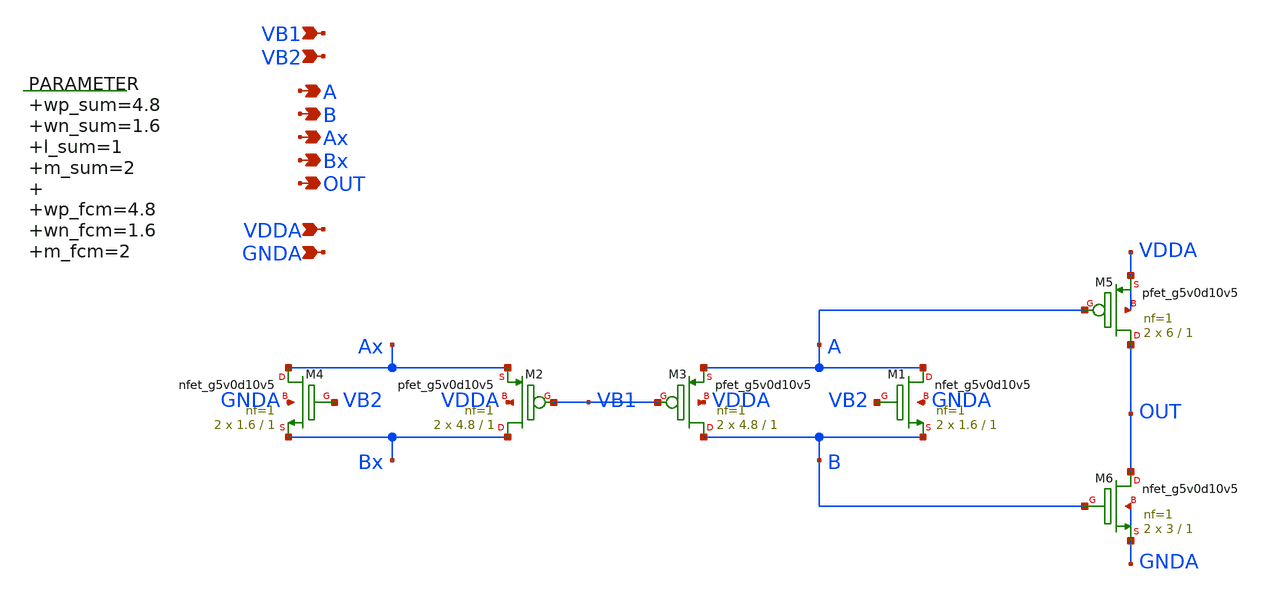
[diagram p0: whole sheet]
** sch_path: xschem/monticelli_top.sch
**.subckt monticelli_top A B VDDA GNDA Ax Bx VB1 VB2 OUT
*.opin A
*.opin B
*.ipin VDDA
*.ipin GNDA
*.opin Ax
*.opin Bx
*.ipin VB1
*.ipin VB2
*.opin OUT
.param wp_sum=4.8 wn_sum=1.6 l_sum=1 m_sum=2 wp_fcm=4.8 wn_fcm=1.6 m_fcm=2

XM1 A VB2 B GNDA sky130_fd_pr__nfet_g5v0d10v5 L=1 W=1.6 nf=1 ad='int((nf+1)/2) * W/nf * 0.29' as='int((nf+2)/2) * W/nf * 0.29'
+ pd='2*int((nf+1)/2) * (W/nf + 0.29)' ps='2*int((nf+2)/2) * (W/nf + 0.29)' nrd='0.29 / W' nrs='0.29 / W'
+ sa=0 sb=0 sd=0 mult=2 m=2
XM2 Bx VB1 Ax VDDA sky130_fd_pr__pfet_g5v0d10v5 L=1 W=4.8 nf=1 ad='int((nf+1)/2) * W/nf * 0.29' as='int((nf+2)/2) * W/nf * 0.29'
+ pd='2*int((nf+1)/2) * (W/nf + 0.29)' ps='2*int((nf+2)/2) * (W/nf + 0.29)' nrd='0.29 / W' nrs='0.29 / W'
+ sa=0 sb=0 sd=0 mult=2 m=2
XM3 B VB1 A VDDA sky130_fd_pr__pfet_g5v0d10v5 L=1 W=4.8 nf=1 ad='int((nf+1)/2) * W/nf * 0.29' as='int((nf+2)/2) * W/nf * 0.29'
+ pd='2*int((nf+1)/2) * (W/nf + 0.29)' ps='2*int((nf+2)/2) * (W/nf + 0.29)' nrd='0.29 / W' nrs='0.29 / W'
+ sa=0 sb=0 sd=0 mult=2 m=2
XM4 Ax VB2 Bx GNDA sky130_fd_pr__nfet_g5v0d10v5 L=1 W=1.6 nf=1 ad='int((nf+1)/2) * W/nf * 0.29' as='int((nf+2)/2) * W/nf * 0.29'
+ pd='2*int((nf+1)/2) * (W/nf + 0.29)' ps='2*int((nf+2)/2) * (W/nf + 0.29)' nrd='0.29 / W' nrs='0.29 / W'
+ sa=0 sb=0 sd=0 mult=2 m=2
XM5 OUT A VDDA VDDA sky130_fd_pr__pfet_g5v0d10v5 L=1 W=6 nf=1 ad='int((nf+1)/2) * W/nf * 0.29' as='int((nf+2)/2) * W/nf * 0.29'
+ pd='2*int((nf+1)/2) * (W/nf + 0.29)' ps='2*int((nf+2)/2) * (W/nf + 0.29)' nrd='0.29 / W' nrs='0.29 / W'
+ sa=0 sb=0 sd=0 mult=2 m=2
XM6 OUT B GNDA GNDA sky130_fd_pr__nfet_g5v0d10v5 L=1 W=3 nf=1 ad='int((nf+1)/2) * W/nf * 0.29' as='int((nf+2)/2) * W/nf * 0.29'
+ pd='2*int((nf+1)/2) * (W/nf + 0.29)' ps='2*int((nf+2)/2) * (W/nf + 0.29)' nrd='0.29 / W' nrs='0.29 / W'
+ sa=0 sb=0 sd=0 mult=2 m=2
**.ends
.end
